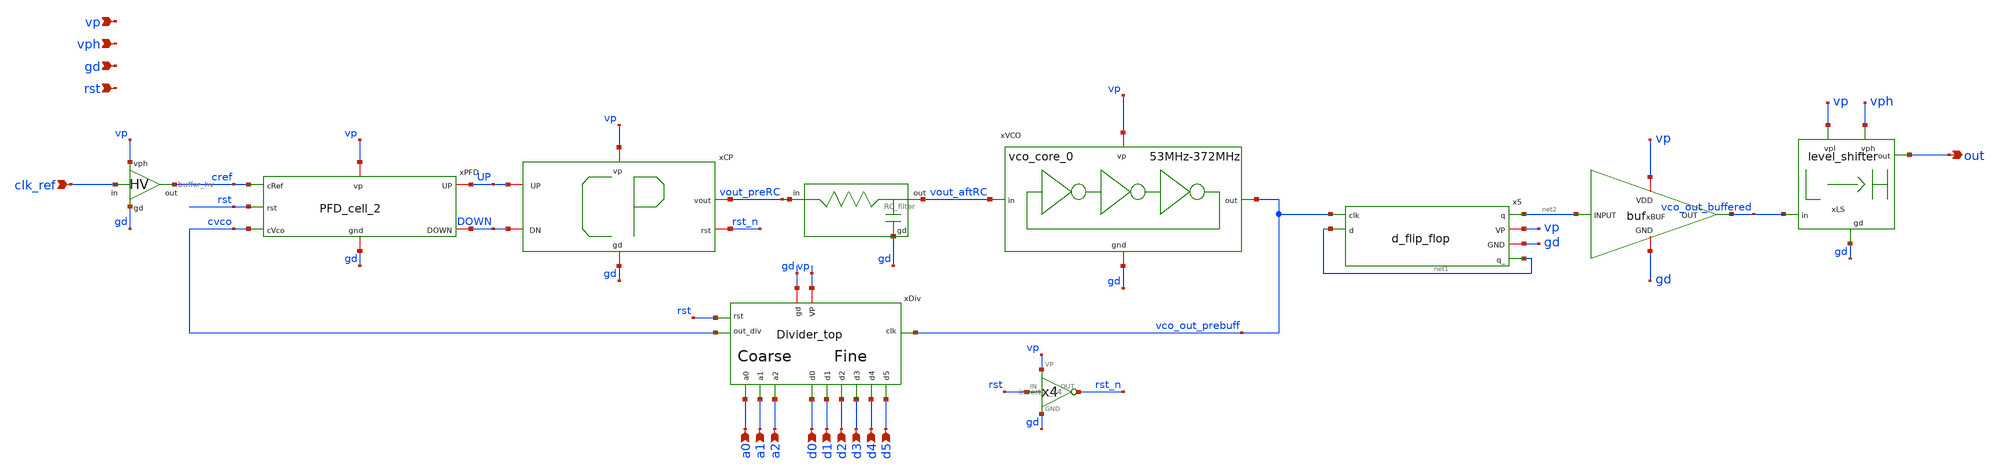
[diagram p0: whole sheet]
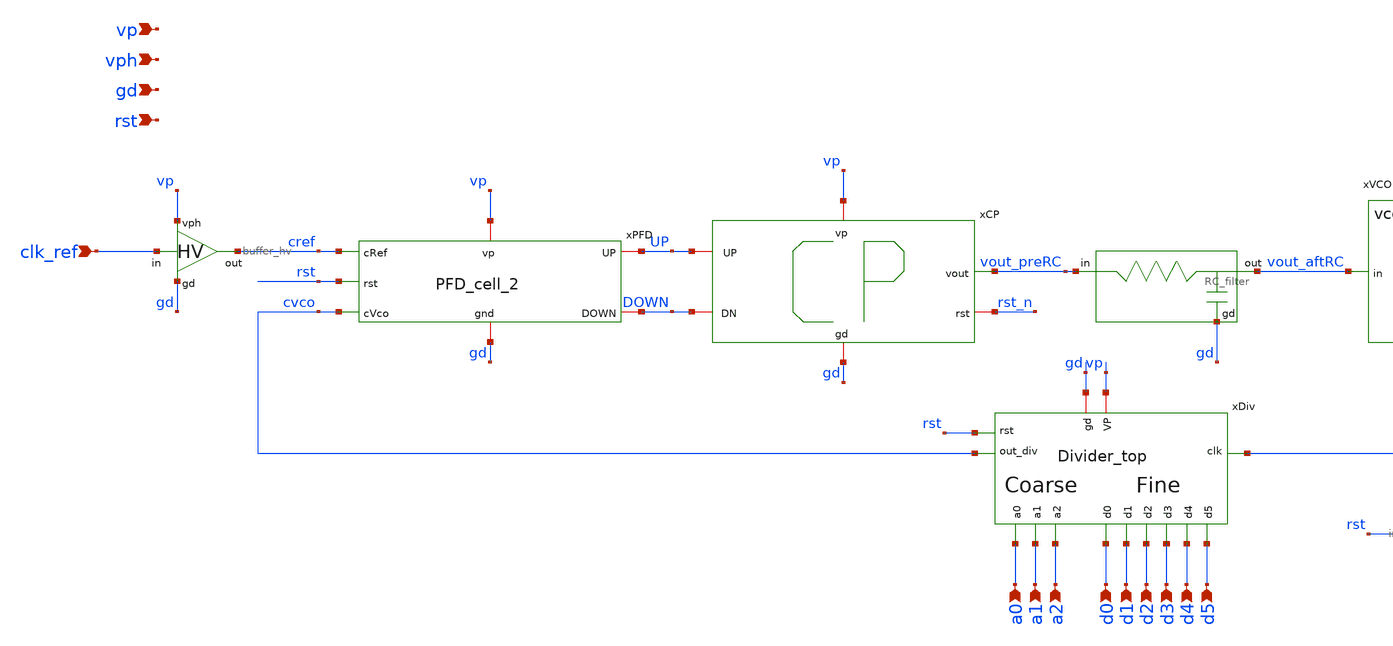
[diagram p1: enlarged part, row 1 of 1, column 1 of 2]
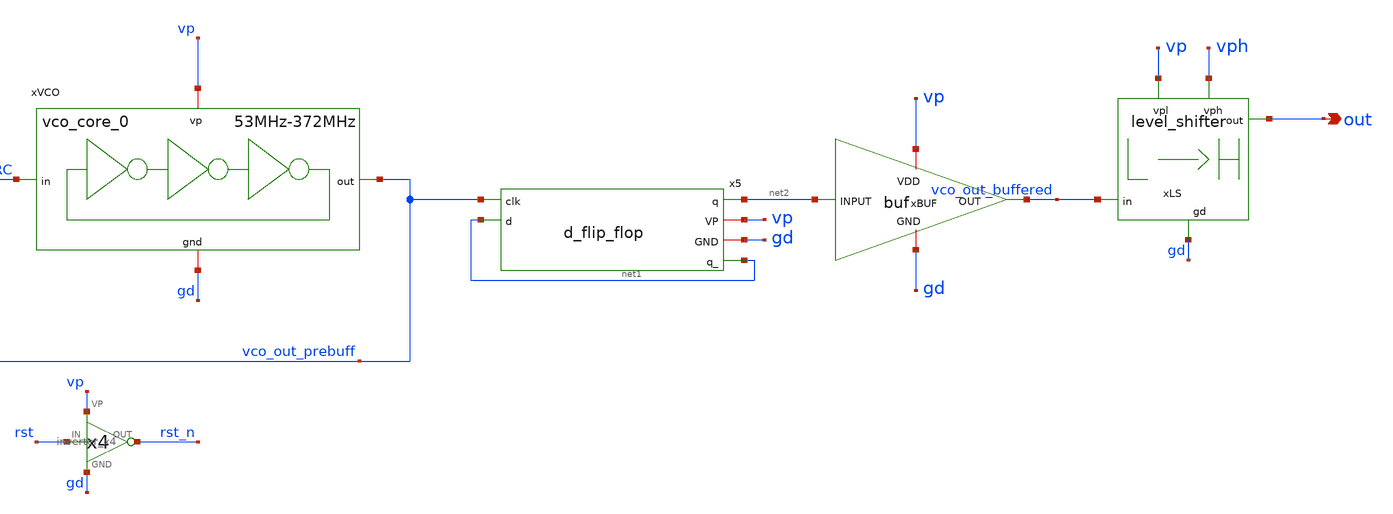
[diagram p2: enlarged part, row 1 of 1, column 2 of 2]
** sch_path: schematics/top/PLL_top.sch
**.subckt PLL_top clk_ref out gd vph vp a0 a1 a2 d0 d1 d2 d3 d4 d5 rst
*.ipin clk_ref
*.opin out
*.ipin gd
*.ipin vph
*.ipin vp
*.ipin a0
*.ipin a1
*.ipin a2
*.ipin d0
*.ipin d1
*.ipin d2
*.ipin d3
*.ipin d4
*.ipin d5
*.ipin rst
xRC vout_aftRC vout_preRC gd RC_filter
x2 vp clk_ref cref gd buffer_hv
xPFD gd vp cref UP DOWN cvco rst PFD_cell_2
xCP vp UP vout_preRC DOWN rst_n gd charge_pump_cell
xBUF vp net2 vco_out_buffered gd buf
xDiv gd vp vco_out_prebuff d0 d1 d2 d3 d4 d5 a0 a1 a2 cvco rst Divider_top
xVCO vp gd vco_out_prebuff vout_aftRC vco_core_0
x5 net2 vp gd net1 vco_out_prebuff net1 d_flip_flop
xLS vph out vp vco_out_buffered gd level_shifter
x10 rst rst_n vp gd inverter_x4
**.ends
.end
